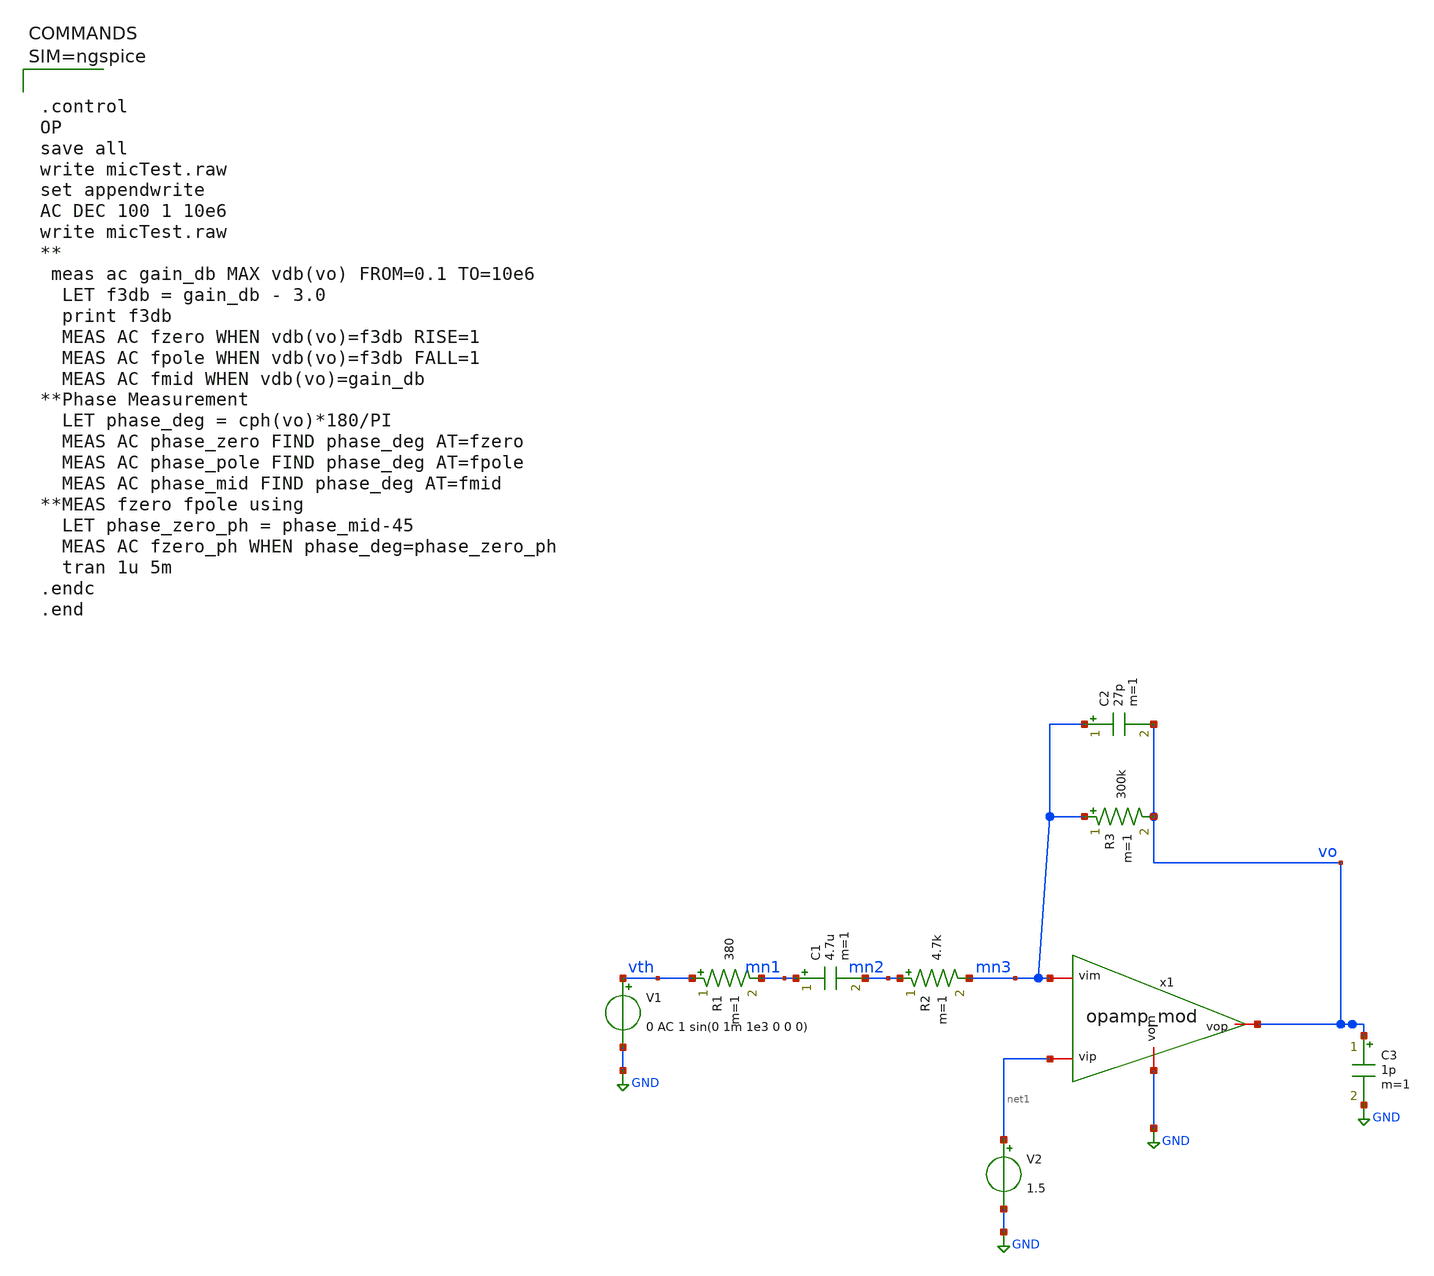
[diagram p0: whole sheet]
** sch_path: xschem/micTestOpamp_mod1.sch
**.subckt micTestOpamp_mod1
V1 vth GND 0 AC 1 sin(0 1m 1e3 0 0 0)
R1 vth mn1 380 m=1
C1 mn1 mn2 4.7u m=1
R2 mn2 mn3 4.7k m=1
R3 mn3 vo 300k m=1
C2 mn3 vo 27p m=1
V2 net1 GND 1.5
C3 vo GND 1p m=1
x1 vo net1 mn3 GND opamp_mod
**** begin user architecture code



.control
OP
save all
write micTest.raw
set appendwrite
AC DEC 100 1 10e6
write micTest.raw
**
 meas ac gain_db MAX vdb(vo) FROM=0.1 TO=10e6
  LET f3db = gain_db - 3.0
  print f3db
  MEAS AC fzero WHEN vdb(vo)=f3db RISE=1
  MEAS AC fpole WHEN vdb(vo)=f3db FALL=1
  MEAS AC fmid WHEN vdb(vo)=gain_db
**Phase Measurement
  LET phase_deg = cph(vo)*180/PI
  MEAS AC phase_zero FIND phase_deg AT=fzero
  MEAS AC phase_pole FIND phase_deg AT=fpole
  MEAS AC phase_mid FIND phase_deg AT=fmid
**MEAS fzero fpole using
  LET phase_zero_ph = phase_mid-45
  MEAS AC fzero_ph WHEN phase_deg=phase_zero_ph
  tran 1u 5m
.endc
.end



**** end user architecture code
**.ends

* expanding   symbol:  opamp_mod.sym # of pins=4
** sym_path: xschem/opamp_mod.sym
** sch_path: xschem/opamp_mod.sch
.subckt opamp_mod vop vip vim vom
*.iopin vop
*.iopin vom
*.iopin vip
*.iopin vim
E1 vop vom vip vim 1000
.ends

.GLOBAL GND
.end
